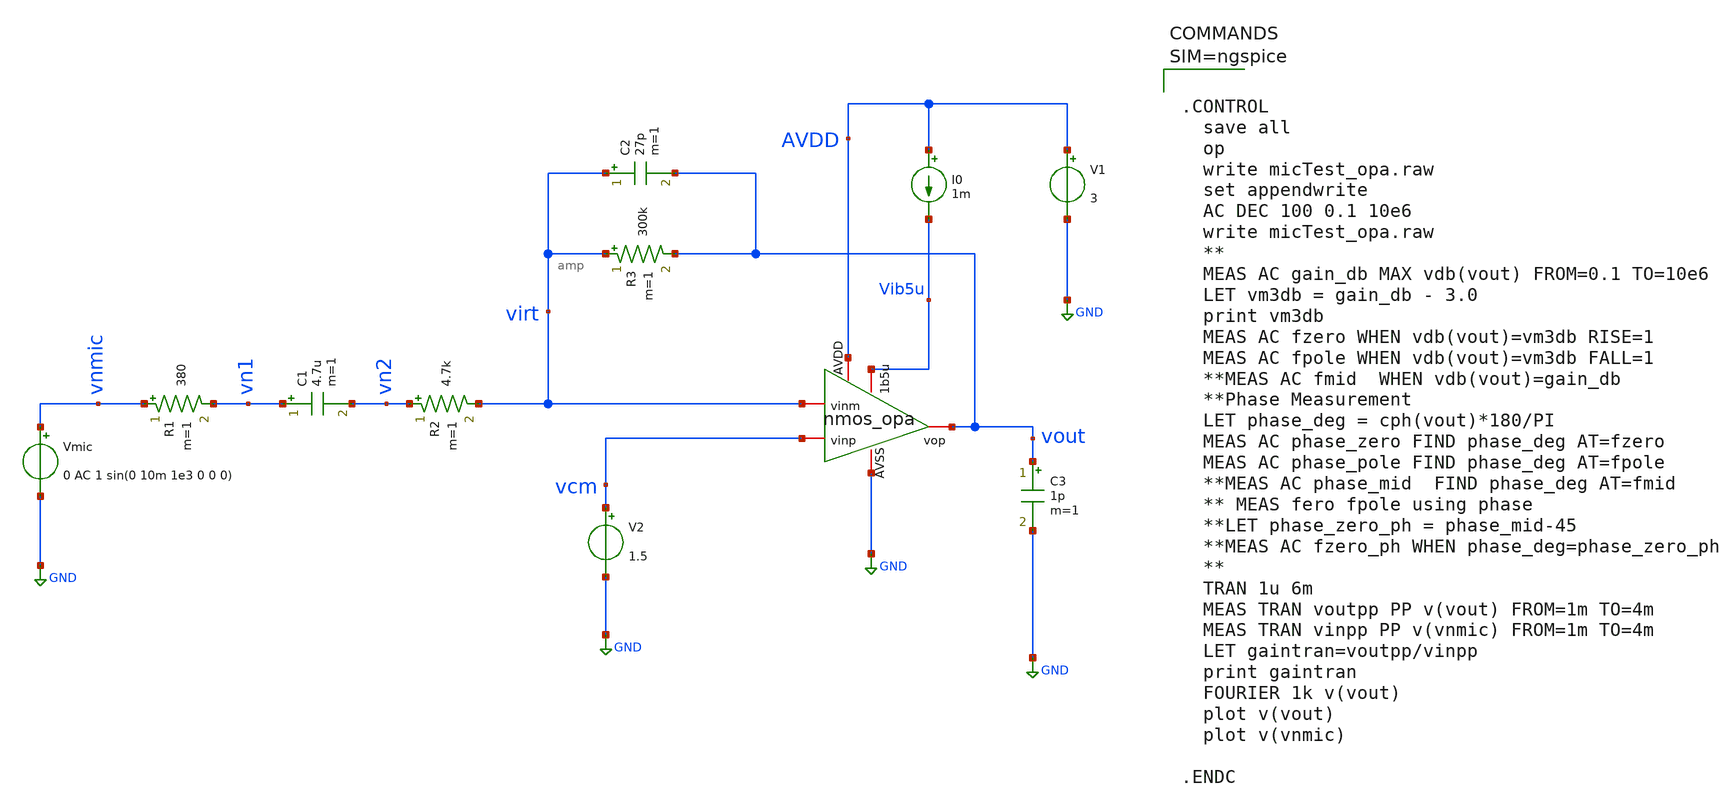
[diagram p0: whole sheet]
** sch_path: work/xschem/mictest_opa_nmos.sch
**.subckt mictest_opa_nmos
Vmic vnmic GND 0 AC 1 sin(0 10m 1e3 0 0 0)
R1 vnmic vn1 380 m=1
R2 vn2 virt 4.7k m=1
C1 vn1 vn2 4.7u m=1
V2 vcm GND 1.5
C2 virt vout 27p m=1
R3 virt vout 300k m=1
C3 vout GND 1p m=1
x1 AVDD vout virt vcm Vib5u GND amp
V1 AVDD GND 3
I0 AVDD Vib5u 1m
**** begin user architecture code



.CONTROL
  save all
  op
  write micTest_opa.raw
  set appendwrite
  AC DEC 100 0.1 10e6
  write micTest_opa.raw
  **
  MEAS AC gain_db MAX vdb(vout) FROM=0.1 TO=10e6
  LET vm3db = gain_db - 3.0
  print vm3db
  MEAS AC fzero WHEN vdb(vout)=vm3db RISE=1
  MEAS AC fpole WHEN vdb(vout)=vm3db FALL=1
  **MEAS AC fmid  WHEN vdb(vout)=gain_db
  **Phase Measurement
  LET phase_deg = cph(vout)*180/PI
  MEAS AC phase_zero FIND phase_deg AT=fzero
  MEAS AC phase_pole FIND phase_deg AT=fpole
  **MEAS AC phase_mid  FIND phase_deg AT=fmid
  ** MEAS fero fpole using phase
  **LET phase_zero_ph = phase_mid-45
  **MEAS AC fzero_ph WHEN phase_deg=phase_zero_ph
  **
  TRAN 1u 6m
  MEAS TRAN voutpp PP v(vout) FROM=1m TO=4m
  MEAS TRAN vinpp PP v(vnmic) FROM=1m TO=4m
  LET gaintran=voutpp/vinpp
  print gaintran
  FOURIER 1k v(vout)
  plot v(vout)
  plot v(vnmic)

.ENDC




** opencircuitdesign pdks install
.lib $::SKYWATER_MODELS/sky130.lib.spice tt

**** end user architecture code
**.ends

* expanding   symbol:  amp.sym # of pins=6
** sym_path: work/xschem/amp.sym
** sch_path: work/xschem/amp.sch
.subckt amp AVDD vop vinm vinp 1b5u AVSS
*.iopin vop
*.iopin vinp
*.iopin vinm
*.iopin 1b5u
*.iopin AVSS
*.iopin AVDD
XMtail net1 1b5u AVSS AVSS sky130_fd_pr__nfet_01v8 L=1 W=5 nf=1 ad='int((1 + 1)/2) * 5 / 1 * 0.29' as='int((1 + 2)/2) * 5 / 1 * 0.29'
+ pd='2*int((1 + 1)/2) * (5 / 1 + 0.29)' ps='2*int((1 + 2)/2) * (5 / 1 + 0.29)' nrd='0.29 / 5 ' nrs='0.29 / 5 '
+ sa=0 sb=0 sd=0 mult=2 m=2
XM1 1b5u 1b5u AVSS AVSS sky130_fd_pr__nfet_01v8 L=1 W=5 nf=1 ad='int((1 + 1)/2) * 5 / 1 * 0.29' as='int((1 + 2)/2) * 5 / 1 * 0.29'
+ pd='2*int((1 + 1)/2) * (5 / 1 + 0.29)' ps='2*int((1 + 2)/2) * (5 / 1 + 0.29)' nrd='0.29 / 5 ' nrs='0.29 / 5 '
+ sa=0 sb=0 sd=0 mult=1 m=1
XMpcmm vop vom AVDD AVDD sky130_fd_pr__pfet_01v8 L=2 W=5 nf=1 ad='int((nf+1)/2) * W/nf * 0.29' as='int((nf+2)/2) * W/nf * 0.29'
+ pd='2*int((nf+1)/2) * (W/nf + 0.29)' ps='2*int((nf+2)/2) * (W/nf + 0.29)' nrd='0.29 / W' nrs='0.29 / W'
+ sa=0 sb=0 sd=0 mult=2 m=2
XMpcmp vom vom AVDD AVDD sky130_fd_pr__pfet_01v8 L=2 W=5 nf=1 ad='int((nf+1)/2) * W/nf * 0.29' as='int((nf+2)/2) * W/nf * 0.29'
+ pd='2*int((nf+1)/2) * (W/nf + 0.29)' ps='2*int((nf+2)/2) * (W/nf + 0.29)' nrd='0.29 / W' nrs='0.29 / W'
+ sa=0 sb=0 sd=0 mult=2 m=2
XMim vop vinm net1 net1 sky130_fd_pr__nfet_01v8 L=2 W=5 nf=1 ad='int((1 + 1)/2) * 5 / 1 * 0.29' as='int((1 + 2)/2) * 5 / 1 * 0.29'
+ pd='2*int((1 + 1)/2) * (5 / 1 + 0.29)' ps='2*int((1 + 2)/2) * (5 / 1 + 0.29)' nrd='0.29 / 5 ' nrs='0.29 / 5 '
+ sa=0 sb=0 sd=0 mult=4 m=4
XMip vom vinp net1 net1 sky130_fd_pr__nfet_01v8 L=2 W=5 nf=1 ad='int((1 + 1)/2) * 5 / 1 * 0.29' as='int((1 + 2)/2) * 5 / 1 * 0.29'
+ pd='2*int((1 + 1)/2) * (5 / 1 + 0.29)' ps='2*int((1 + 2)/2) * (5 / 1 + 0.29)' nrd='0.29 / 5 ' nrs='0.29 / 5 '
+ sa=0 sb=0 sd=0 mult=4 m=4
**** begin user architecture code



* ngspice commands
.control
save all
write amp.raw
set appendfile
write amp.raw

.endc



**** end user architecture code
.ends

.GLOBAL GND
.end
